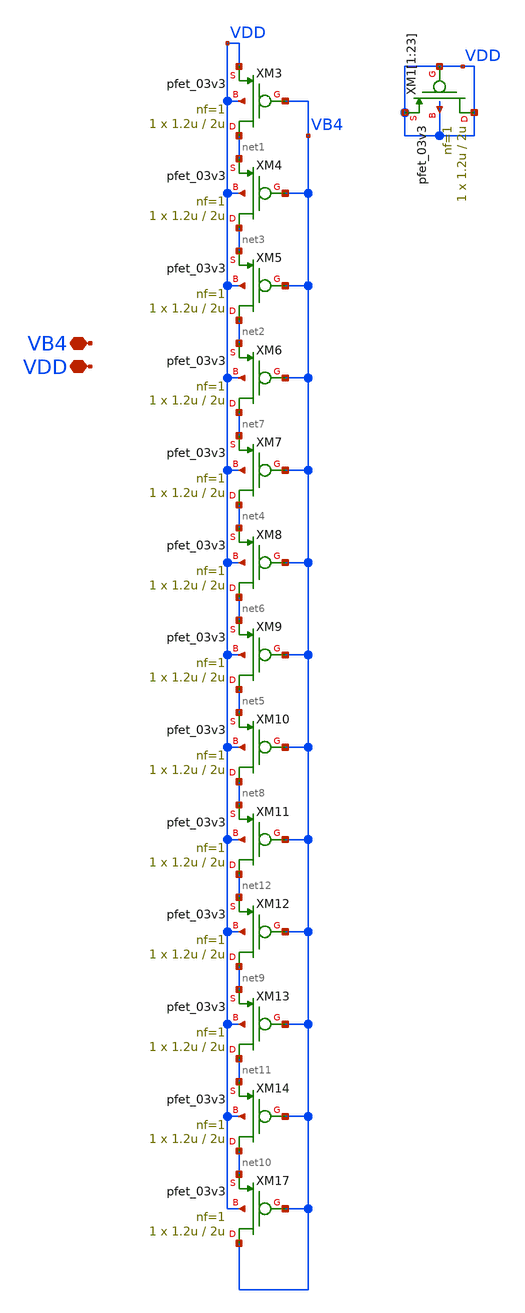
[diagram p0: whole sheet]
** sch_path: Voltage_Reference/LDO/Folded/FC_bias_vb4.sch
**.subckt FC_bias_vb4 VDD VB4
*.iopin VDD
*.iopin VB4
XM3 net1 VB4 VDD VDD pfet_03v3 L=2u W=1.2u nf=1 ad='int((nf+1)/2) * W/nf * 0.18u' as='int((nf+2)/2) * W/nf * 0.18u'
+ pd='2*int((nf+1)/2) * (W/nf + 0.18u)' ps='2*int((nf+2)/2) * (W/nf + 0.18u)' nrd='0.18u / W' nrs='0.18u / W'
+ sa=0 sb=0 sd=0 m=1
XM4 net3 VB4 net1 VDD pfet_03v3 L=2u W=1.2u nf=1 ad='int((nf+1)/2) * W/nf * 0.18u' as='int((nf+2)/2) * W/nf * 0.18u'
+ pd='2*int((nf+1)/2) * (W/nf + 0.18u)' ps='2*int((nf+2)/2) * (W/nf + 0.18u)' nrd='0.18u / W' nrs='0.18u / W'
+ sa=0 sb=0 sd=0 m=1
XM5 net2 VB4 net3 VDD pfet_03v3 L=2u W=1.2u nf=1 ad='int((nf+1)/2) * W/nf * 0.18u' as='int((nf+2)/2) * W/nf * 0.18u'
+ pd='2*int((nf+1)/2) * (W/nf + 0.18u)' ps='2*int((nf+2)/2) * (W/nf + 0.18u)' nrd='0.18u / W' nrs='0.18u / W'
+ sa=0 sb=0 sd=0 m=1
XM6 net7 VB4 net2 VDD pfet_03v3 L=2u W=1.2u nf=1 ad='int((nf+1)/2) * W/nf * 0.18u' as='int((nf+2)/2) * W/nf * 0.18u'
+ pd='2*int((nf+1)/2) * (W/nf + 0.18u)' ps='2*int((nf+2)/2) * (W/nf + 0.18u)' nrd='0.18u / W' nrs='0.18u / W'
+ sa=0 sb=0 sd=0 m=1
XM7 net4 VB4 net7 VDD pfet_03v3 L=2u W=1.2u nf=1 ad='int((nf+1)/2) * W/nf * 0.18u' as='int((nf+2)/2) * W/nf * 0.18u'
+ pd='2*int((nf+1)/2) * (W/nf + 0.18u)' ps='2*int((nf+2)/2) * (W/nf + 0.18u)' nrd='0.18u / W' nrs='0.18u / W'
+ sa=0 sb=0 sd=0 m=1
XM8 net6 VB4 net4 VDD pfet_03v3 L=2u W=1.2u nf=1 ad='int((nf+1)/2) * W/nf * 0.18u' as='int((nf+2)/2) * W/nf * 0.18u'
+ pd='2*int((nf+1)/2) * (W/nf + 0.18u)' ps='2*int((nf+2)/2) * (W/nf + 0.18u)' nrd='0.18u / W' nrs='0.18u / W'
+ sa=0 sb=0 sd=0 m=1
XM9 net5 VB4 net6 VDD pfet_03v3 L=2u W=1.2u nf=1 ad='int((nf+1)/2) * W/nf * 0.18u' as='int((nf+2)/2) * W/nf * 0.18u'
+ pd='2*int((nf+1)/2) * (W/nf + 0.18u)' ps='2*int((nf+2)/2) * (W/nf + 0.18u)' nrd='0.18u / W' nrs='0.18u / W'
+ sa=0 sb=0 sd=0 m=1
XM10 net8 VB4 net5 VDD pfet_03v3 L=2u W=1.2u nf=1 ad='int((nf+1)/2) * W/nf * 0.18u' as='int((nf+2)/2) * W/nf * 0.18u'
+ pd='2*int((nf+1)/2) * (W/nf + 0.18u)' ps='2*int((nf+2)/2) * (W/nf + 0.18u)' nrd='0.18u / W' nrs='0.18u / W'
+ sa=0 sb=0 sd=0 m=1
XM11 net12 VB4 net8 VDD pfet_03v3 L=2u W=1.2u nf=1 ad='int((nf+1)/2) * W/nf * 0.18u' as='int((nf+2)/2) * W/nf * 0.18u'
+ pd='2*int((nf+1)/2) * (W/nf + 0.18u)' ps='2*int((nf+2)/2) * (W/nf + 0.18u)' nrd='0.18u / W' nrs='0.18u / W'
+ sa=0 sb=0 sd=0 m=1
XM12 net9 VB4 net12 VDD pfet_03v3 L=2u W=1.2u nf=1 ad='int((nf+1)/2) * W/nf * 0.18u' as='int((nf+2)/2) * W/nf * 0.18u'
+ pd='2*int((nf+1)/2) * (W/nf + 0.18u)' ps='2*int((nf+2)/2) * (W/nf + 0.18u)' nrd='0.18u / W' nrs='0.18u / W'
+ sa=0 sb=0 sd=0 m=1
XM13 net11 VB4 net9 VDD pfet_03v3 L=2u W=1.2u nf=1 ad='int((nf+1)/2) * W/nf * 0.18u' as='int((nf+2)/2) * W/nf * 0.18u'
+ pd='2*int((nf+1)/2) * (W/nf + 0.18u)' ps='2*int((nf+2)/2) * (W/nf + 0.18u)' nrd='0.18u / W' nrs='0.18u / W'
+ sa=0 sb=0 sd=0 m=1
XM14 net10 VB4 net11 VDD pfet_03v3 L=2u W=1.2u nf=1 ad='int((nf+1)/2) * W/nf * 0.18u' as='int((nf+2)/2) * W/nf * 0.18u'
+ pd='2*int((nf+1)/2) * (W/nf + 0.18u)' ps='2*int((nf+2)/2) * (W/nf + 0.18u)' nrd='0.18u / W' nrs='0.18u / W'
+ sa=0 sb=0 sd=0 m=1
XM17 VB4 VB4 net10 VDD pfet_03v3 L=2u W=1.2u nf=1 ad='int((nf+1)/2) * W/nf * 0.18u' as='int((nf+2)/2) * W/nf * 0.18u'
+ pd='2*int((nf+1)/2) * (W/nf + 0.18u)' ps='2*int((nf+2)/2) * (W/nf + 0.18u)' nrd='0.18u / W' nrs='0.18u / W'
+ sa=0 sb=0 sd=0 m=1
XM1[1] VDD VDD VDD VDD pfet_03v3 L=2u W=1.2u nf=1 ad='int((nf+1)/2) * W/nf * 0.18u' as='int((nf+2)/2) * W/nf * 0.18u'
+ pd='2*int((nf+1)/2) * (W/nf + 0.18u)' ps='2*int((nf+2)/2) * (W/nf + 0.18u)' nrd='0.18u / W' nrs='0.18u / W'
+ sa=0 sb=0 sd=0 m=1
XM1[2] VDD VDD VDD VDD pfet_03v3 L=2u W=1.2u nf=1 ad='int((nf+1)/2) * W/nf * 0.18u' as='int((nf+2)/2) * W/nf * 0.18u'
+ pd='2*int((nf+1)/2) * (W/nf + 0.18u)' ps='2*int((nf+2)/2) * (W/nf + 0.18u)' nrd='0.18u / W' nrs='0.18u / W'
+ sa=0 sb=0 sd=0 m=1
XM1[3] VDD VDD VDD VDD pfet_03v3 L=2u W=1.2u nf=1 ad='int((nf+1)/2) * W/nf * 0.18u' as='int((nf+2)/2) * W/nf * 0.18u'
+ pd='2*int((nf+1)/2) * (W/nf + 0.18u)' ps='2*int((nf+2)/2) * (W/nf + 0.18u)' nrd='0.18u / W' nrs='0.18u / W'
+ sa=0 sb=0 sd=0 m=1
XM1[4] VDD VDD VDD VDD pfet_03v3 L=2u W=1.2u nf=1 ad='int((nf+1)/2) * W/nf * 0.18u' as='int((nf+2)/2) * W/nf * 0.18u'
+ pd='2*int((nf+1)/2) * (W/nf + 0.18u)' ps='2*int((nf+2)/2) * (W/nf + 0.18u)' nrd='0.18u / W' nrs='0.18u / W'
+ sa=0 sb=0 sd=0 m=1
XM1[5] VDD VDD VDD VDD pfet_03v3 L=2u W=1.2u nf=1 ad='int((nf+1)/2) * W/nf * 0.18u' as='int((nf+2)/2) * W/nf * 0.18u'
+ pd='2*int((nf+1)/2) * (W/nf + 0.18u)' ps='2*int((nf+2)/2) * (W/nf + 0.18u)' nrd='0.18u / W' nrs='0.18u / W'
+ sa=0 sb=0 sd=0 m=1
XM1[6] VDD VDD VDD VDD pfet_03v3 L=2u W=1.2u nf=1 ad='int((nf+1)/2) * W/nf * 0.18u' as='int((nf+2)/2) * W/nf * 0.18u'
+ pd='2*int((nf+1)/2) * (W/nf + 0.18u)' ps='2*int((nf+2)/2) * (W/nf + 0.18u)' nrd='0.18u / W' nrs='0.18u / W'
+ sa=0 sb=0 sd=0 m=1
XM1[7] VDD VDD VDD VDD pfet_03v3 L=2u W=1.2u nf=1 ad='int((nf+1)/2) * W/nf * 0.18u' as='int((nf+2)/2) * W/nf * 0.18u'
+ pd='2*int((nf+1)/2) * (W/nf + 0.18u)' ps='2*int((nf+2)/2) * (W/nf + 0.18u)' nrd='0.18u / W' nrs='0.18u / W'
+ sa=0 sb=0 sd=0 m=1
XM1[8] VDD VDD VDD VDD pfet_03v3 L=2u W=1.2u nf=1 ad='int((nf+1)/2) * W/nf * 0.18u' as='int((nf+2)/2) * W/nf * 0.18u'
+ pd='2*int((nf+1)/2) * (W/nf + 0.18u)' ps='2*int((nf+2)/2) * (W/nf + 0.18u)' nrd='0.18u / W' nrs='0.18u / W'
+ sa=0 sb=0 sd=0 m=1
XM1[9] VDD VDD VDD VDD pfet_03v3 L=2u W=1.2u nf=1 ad='int((nf+1)/2) * W/nf * 0.18u' as='int((nf+2)/2) * W/nf * 0.18u'
+ pd='2*int((nf+1)/2) * (W/nf + 0.18u)' ps='2*int((nf+2)/2) * (W/nf + 0.18u)' nrd='0.18u / W' nrs='0.18u / W'
+ sa=0 sb=0 sd=0 m=1
XM1[10] VDD VDD VDD VDD pfet_03v3 L=2u W=1.2u nf=1 ad='int((nf+1)/2) * W/nf * 0.18u' as='int((nf+2)/2) * W/nf * 0.18u'
+ pd='2*int((nf+1)/2) * (W/nf + 0.18u)' ps='2*int((nf+2)/2) * (W/nf + 0.18u)' nrd='0.18u / W' nrs='0.18u / W'
+ sa=0 sb=0 sd=0 m=1
XM1[11] VDD VDD VDD VDD pfet_03v3 L=2u W=1.2u nf=1 ad='int((nf+1)/2) * W/nf * 0.18u' as='int((nf+2)/2) * W/nf * 0.18u'
+ pd='2*int((nf+1)/2) * (W/nf + 0.18u)' ps='2*int((nf+2)/2) * (W/nf + 0.18u)' nrd='0.18u / W' nrs='0.18u / W'
+ sa=0 sb=0 sd=0 m=1
XM1[12] VDD VDD VDD VDD pfet_03v3 L=2u W=1.2u nf=1 ad='int((nf+1)/2) * W/nf * 0.18u' as='int((nf+2)/2) * W/nf * 0.18u'
+ pd='2*int((nf+1)/2) * (W/nf + 0.18u)' ps='2*int((nf+2)/2) * (W/nf + 0.18u)' nrd='0.18u / W' nrs='0.18u / W'
+ sa=0 sb=0 sd=0 m=1
XM1[13] VDD VDD VDD VDD pfet_03v3 L=2u W=1.2u nf=1 ad='int((nf+1)/2) * W/nf * 0.18u' as='int((nf+2)/2) * W/nf * 0.18u'
+ pd='2*int((nf+1)/2) * (W/nf + 0.18u)' ps='2*int((nf+2)/2) * (W/nf + 0.18u)' nrd='0.18u / W' nrs='0.18u / W'
+ sa=0 sb=0 sd=0 m=1
XM1[14] VDD VDD VDD VDD pfet_03v3 L=2u W=1.2u nf=1 ad='int((nf+1)/2) * W/nf * 0.18u' as='int((nf+2)/2) * W/nf * 0.18u'
+ pd='2*int((nf+1)/2) * (W/nf + 0.18u)' ps='2*int((nf+2)/2) * (W/nf + 0.18u)' nrd='0.18u / W' nrs='0.18u / W'
+ sa=0 sb=0 sd=0 m=1
XM1[15] VDD VDD VDD VDD pfet_03v3 L=2u W=1.2u nf=1 ad='int((nf+1)/2) * W/nf * 0.18u' as='int((nf+2)/2) * W/nf * 0.18u'
+ pd='2*int((nf+1)/2) * (W/nf + 0.18u)' ps='2*int((nf+2)/2) * (W/nf + 0.18u)' nrd='0.18u / W' nrs='0.18u / W'
+ sa=0 sb=0 sd=0 m=1
XM1[16] VDD VDD VDD VDD pfet_03v3 L=2u W=1.2u nf=1 ad='int((nf+1)/2) * W/nf * 0.18u' as='int((nf+2)/2) * W/nf * 0.18u'
+ pd='2*int((nf+1)/2) * (W/nf + 0.18u)' ps='2*int((nf+2)/2) * (W/nf + 0.18u)' nrd='0.18u / W' nrs='0.18u / W'
+ sa=0 sb=0 sd=0 m=1
XM1[17] VDD VDD VDD VDD pfet_03v3 L=2u W=1.2u nf=1 ad='int((nf+1)/2) * W/nf * 0.18u' as='int((nf+2)/2) * W/nf * 0.18u'
+ pd='2*int((nf+1)/2) * (W/nf + 0.18u)' ps='2*int((nf+2)/2) * (W/nf + 0.18u)' nrd='0.18u / W' nrs='0.18u / W'
+ sa=0 sb=0 sd=0 m=1
XM1[18] VDD VDD VDD VDD pfet_03v3 L=2u W=1.2u nf=1 ad='int((nf+1)/2) * W/nf * 0.18u' as='int((nf+2)/2) * W/nf * 0.18u'
+ pd='2*int((nf+1)/2) * (W/nf + 0.18u)' ps='2*int((nf+2)/2) * (W/nf + 0.18u)' nrd='0.18u / W' nrs='0.18u / W'
+ sa=0 sb=0 sd=0 m=1
XM1[19] VDD VDD VDD VDD pfet_03v3 L=2u W=1.2u nf=1 ad='int((nf+1)/2) * W/nf * 0.18u' as='int((nf+2)/2) * W/nf * 0.18u'
+ pd='2*int((nf+1)/2) * (W/nf + 0.18u)' ps='2*int((nf+2)/2) * (W/nf + 0.18u)' nrd='0.18u / W' nrs='0.18u / W'
+ sa=0 sb=0 sd=0 m=1
XM1[20] VDD VDD VDD VDD pfet_03v3 L=2u W=1.2u nf=1 ad='int((nf+1)/2) * W/nf * 0.18u' as='int((nf+2)/2) * W/nf * 0.18u'
+ pd='2*int((nf+1)/2) * (W/nf + 0.18u)' ps='2*int((nf+2)/2) * (W/nf + 0.18u)' nrd='0.18u / W' nrs='0.18u / W'
+ sa=0 sb=0 sd=0 m=1
XM1[21] VDD VDD VDD VDD pfet_03v3 L=2u W=1.2u nf=1 ad='int((nf+1)/2) * W/nf * 0.18u' as='int((nf+2)/2) * W/nf * 0.18u'
+ pd='2*int((nf+1)/2) * (W/nf + 0.18u)' ps='2*int((nf+2)/2) * (W/nf + 0.18u)' nrd='0.18u / W' nrs='0.18u / W'
+ sa=0 sb=0 sd=0 m=1
XM1[22] VDD VDD VDD VDD pfet_03v3 L=2u W=1.2u nf=1 ad='int((nf+1)/2) * W/nf * 0.18u' as='int((nf+2)/2) * W/nf * 0.18u'
+ pd='2*int((nf+1)/2) * (W/nf + 0.18u)' ps='2*int((nf+2)/2) * (W/nf + 0.18u)' nrd='0.18u / W' nrs='0.18u / W'
+ sa=0 sb=0 sd=0 m=1
XM1[23] VDD VDD VDD VDD pfet_03v3 L=2u W=1.2u nf=1 ad='int((nf+1)/2) * W/nf * 0.18u' as='int((nf+2)/2) * W/nf * 0.18u'
+ pd='2*int((nf+1)/2) * (W/nf + 0.18u)' ps='2*int((nf+2)/2) * (W/nf + 0.18u)' nrd='0.18u / W' nrs='0.18u / W'
+ sa=0 sb=0 sd=0 m=1
**.ends
.end
